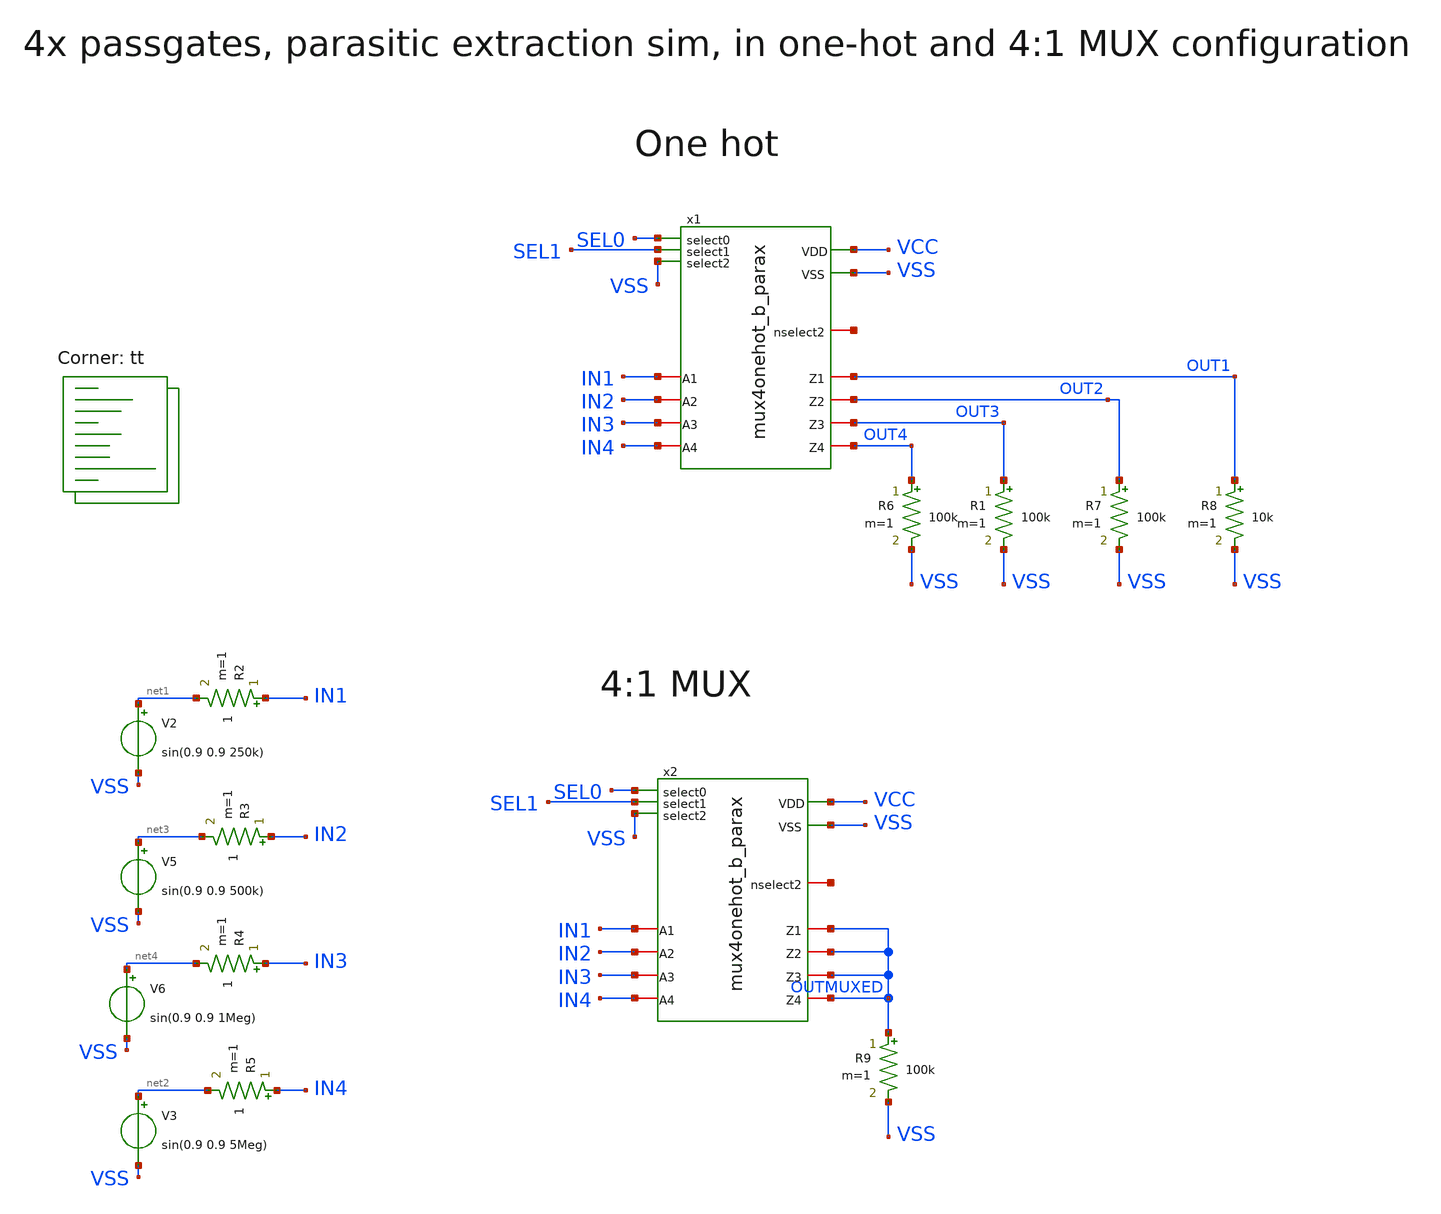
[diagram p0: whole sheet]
** sch_path: xschem/tb_4muxonehot_b.sch
**.subckt tb_4muxonehot_b
V2 net1 VSS sin(0.9 0.9 250k)
V3 net2 VSS sin(0.9 0.9 5Meg)
V5 net3 VSS sin(0.9 0.9 500k)
V6 net4 VSS sin(0.9 0.9 1Meg)
R2 IN1 net1 1 m=1
R3 IN2 net3 1 m=1
R4 IN3 net4 1 m=1
R5 IN4 net2 1 m=1
R6 OUT4 VSS 100k m=1
R1 OUT3 VSS 100k m=1
R7 OUT2 VSS 100k m=1
R8 OUT1 VSS 10k m=1
R9 OUTMUXED VSS 100k m=1
x1 SEL1 VCC VSS IN3 IN2 IN1 OUT3 OUT1 OUT2 IN4 OUT4 SEL0 VSS net5 mux4onehot_b_parax
x2 SEL1 VCC VSS IN3 IN2 IN1 OUTMUXED OUTMUXED OUTMUXED IN4 OUTMUXED SEL0 VSS net6 mux4onehot_b_parax
**** begin user architecture code
.lib $::SKYWATER_MODELS/sky130.lib.spice tt
**** end user architecture code
**.ends

* expanding   symbol:  /home/ttuser/vmswap/tt09-analogmux/xschem/mux4onehot_b_parax.sym # of pins=14
** sym_path: xschem/mux4onehot_b.sym
.include [file normalize extracted/mux4onehot_b_parax.spice]
**** begin user architecture code


* ngspice commands
* .options savecurrents
.param VCC = 1.8
.param SRCRES = 1k
.include stimuli_tb_4muxonehot_b.cir
.control
save all
op
write tb_4muxonehot_b.raw
set appendwrite
tran 50n 80u
write tb_4muxonehot_b.raw
* quit 0
.endc



**** end user architecture code
.end
